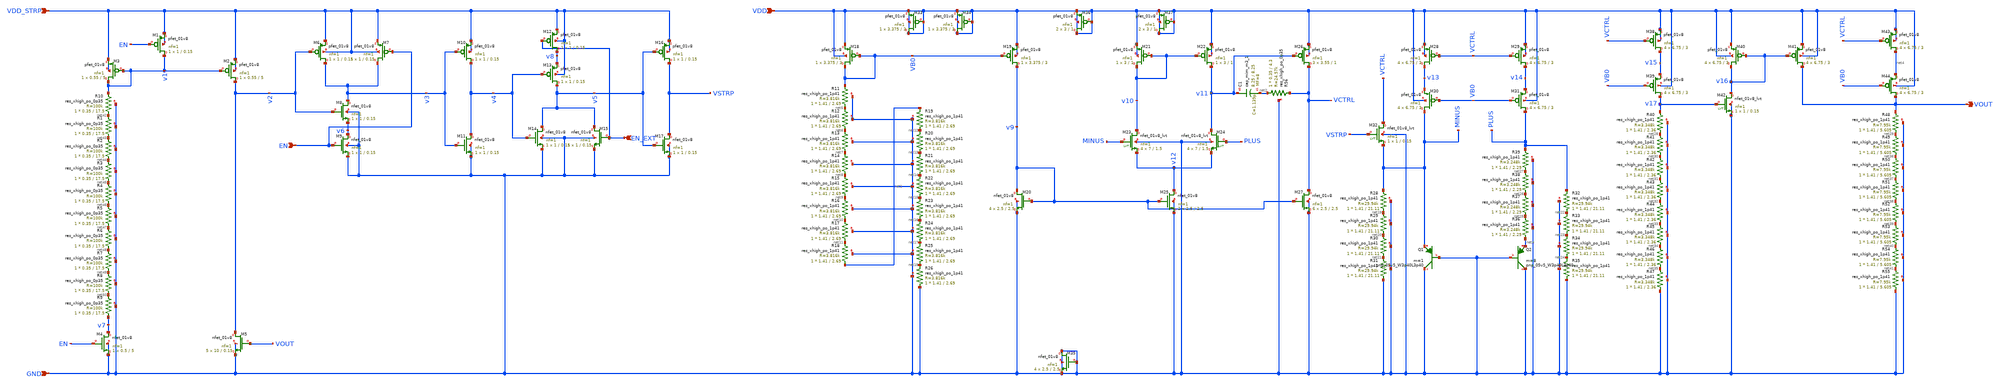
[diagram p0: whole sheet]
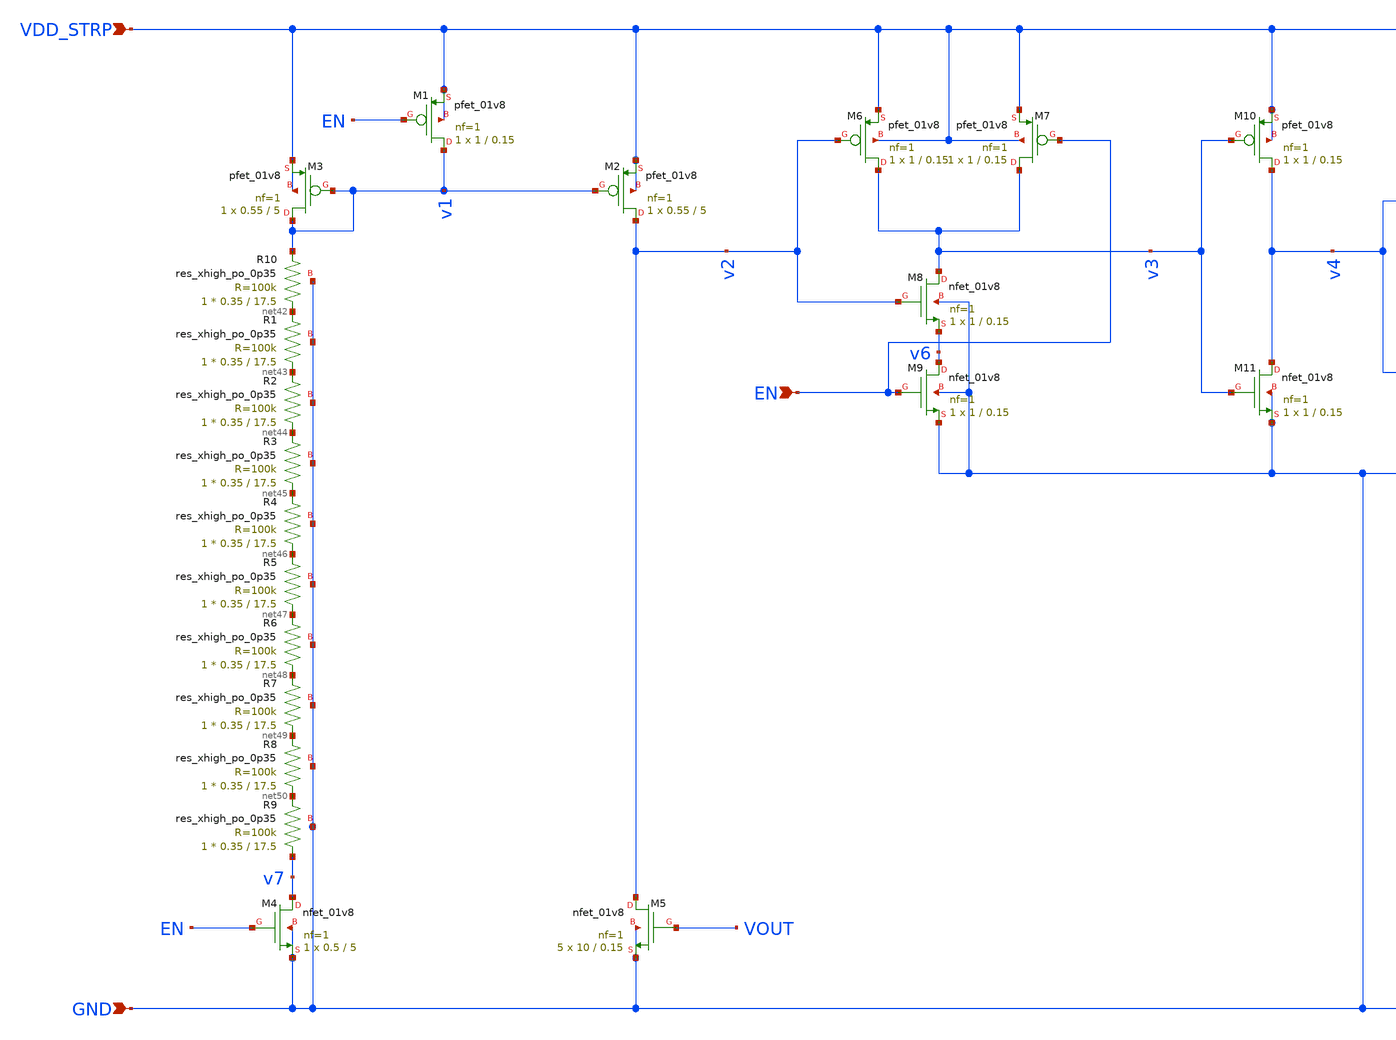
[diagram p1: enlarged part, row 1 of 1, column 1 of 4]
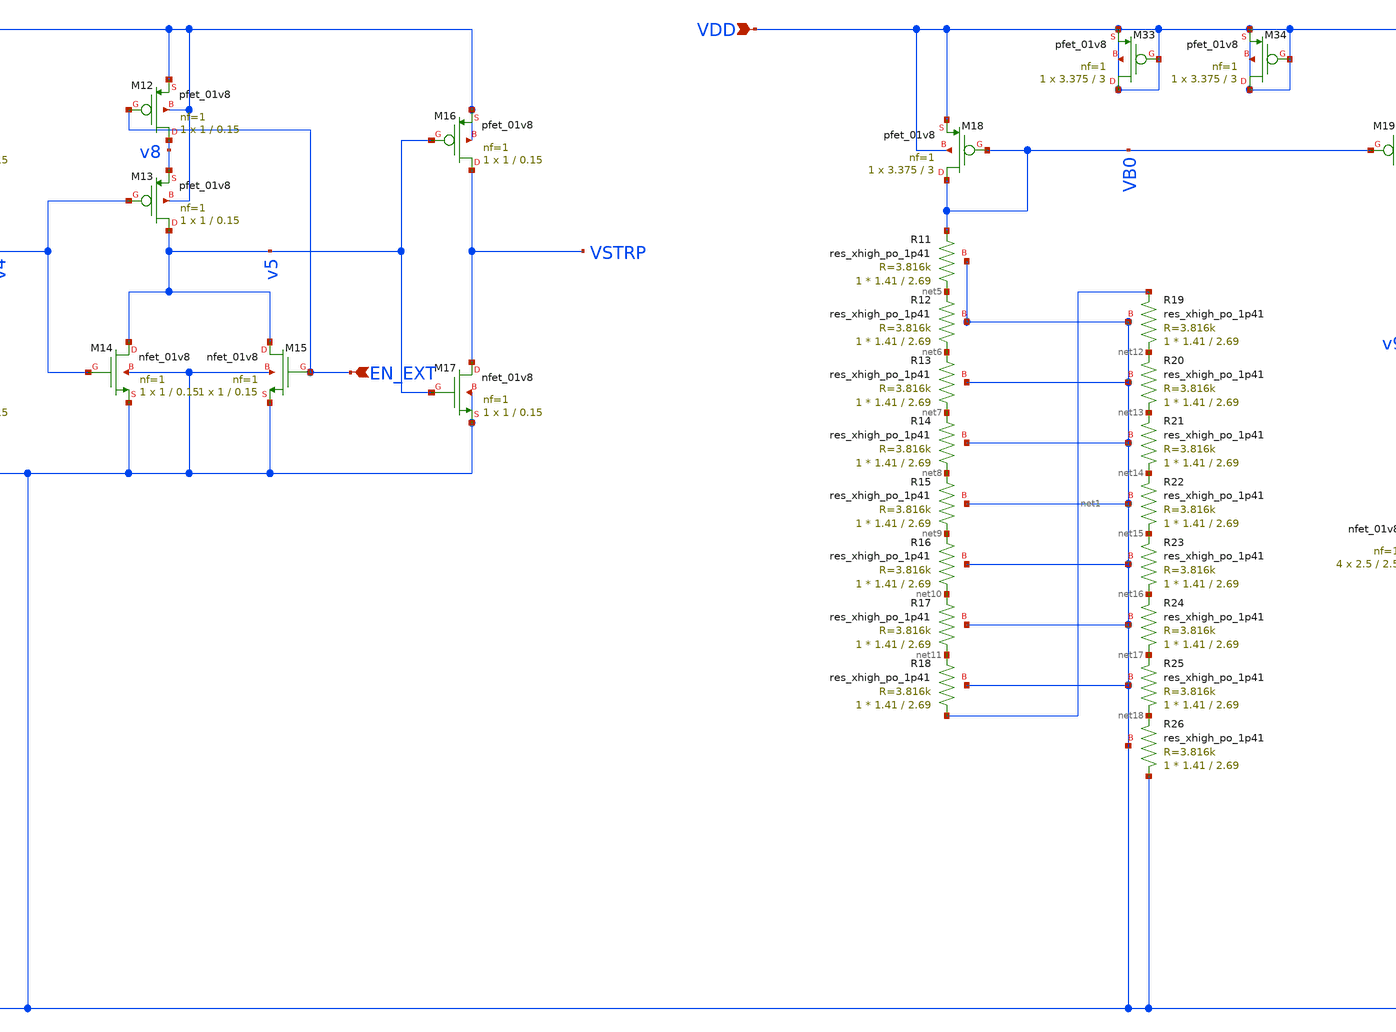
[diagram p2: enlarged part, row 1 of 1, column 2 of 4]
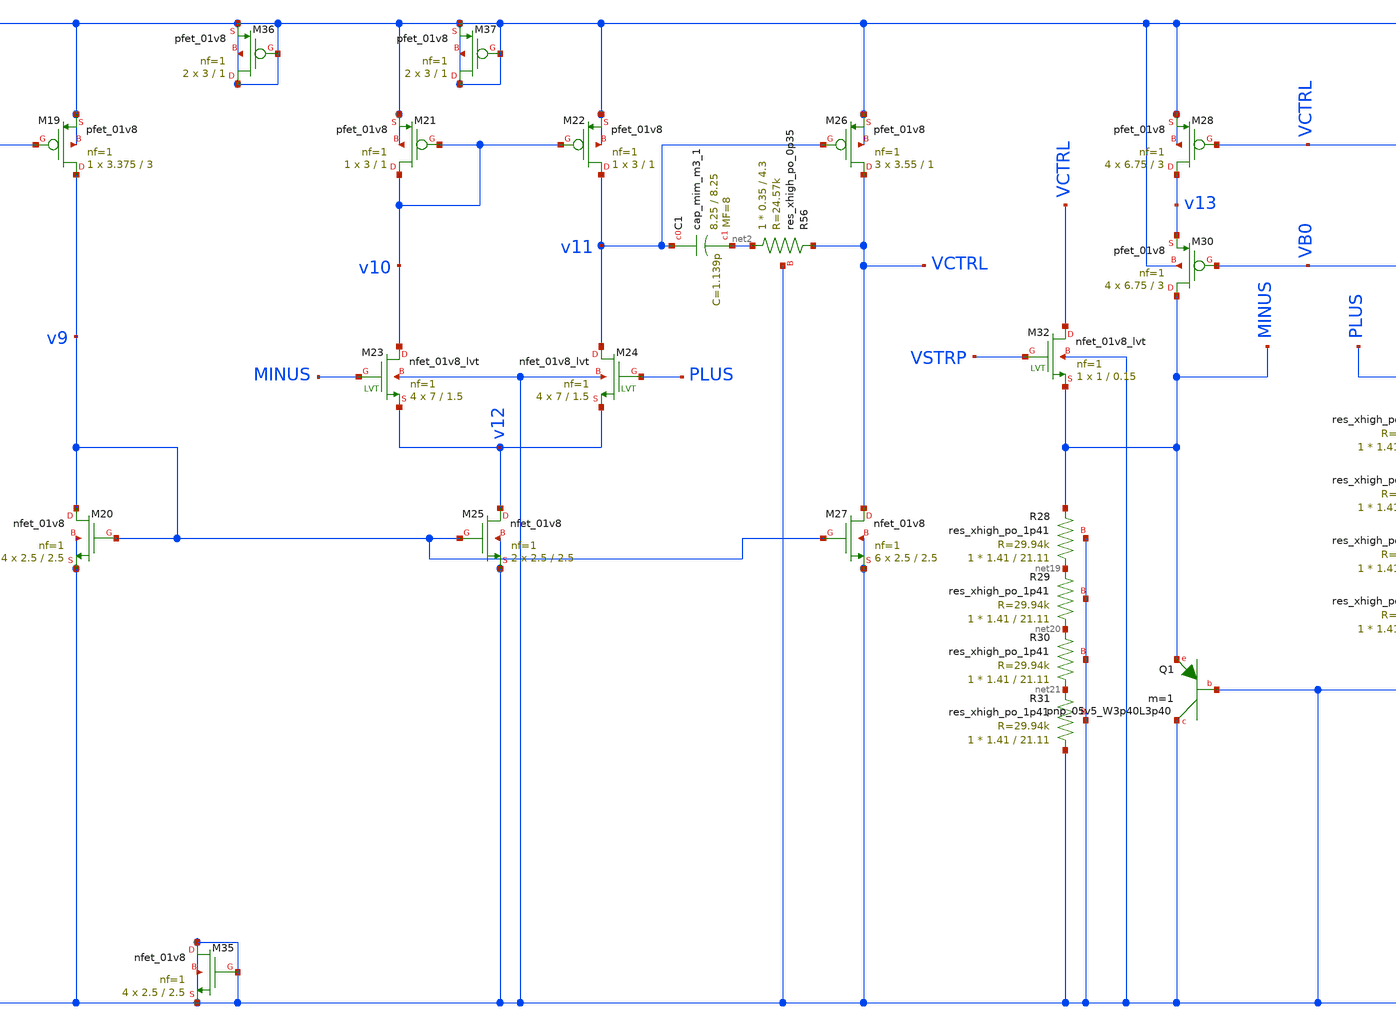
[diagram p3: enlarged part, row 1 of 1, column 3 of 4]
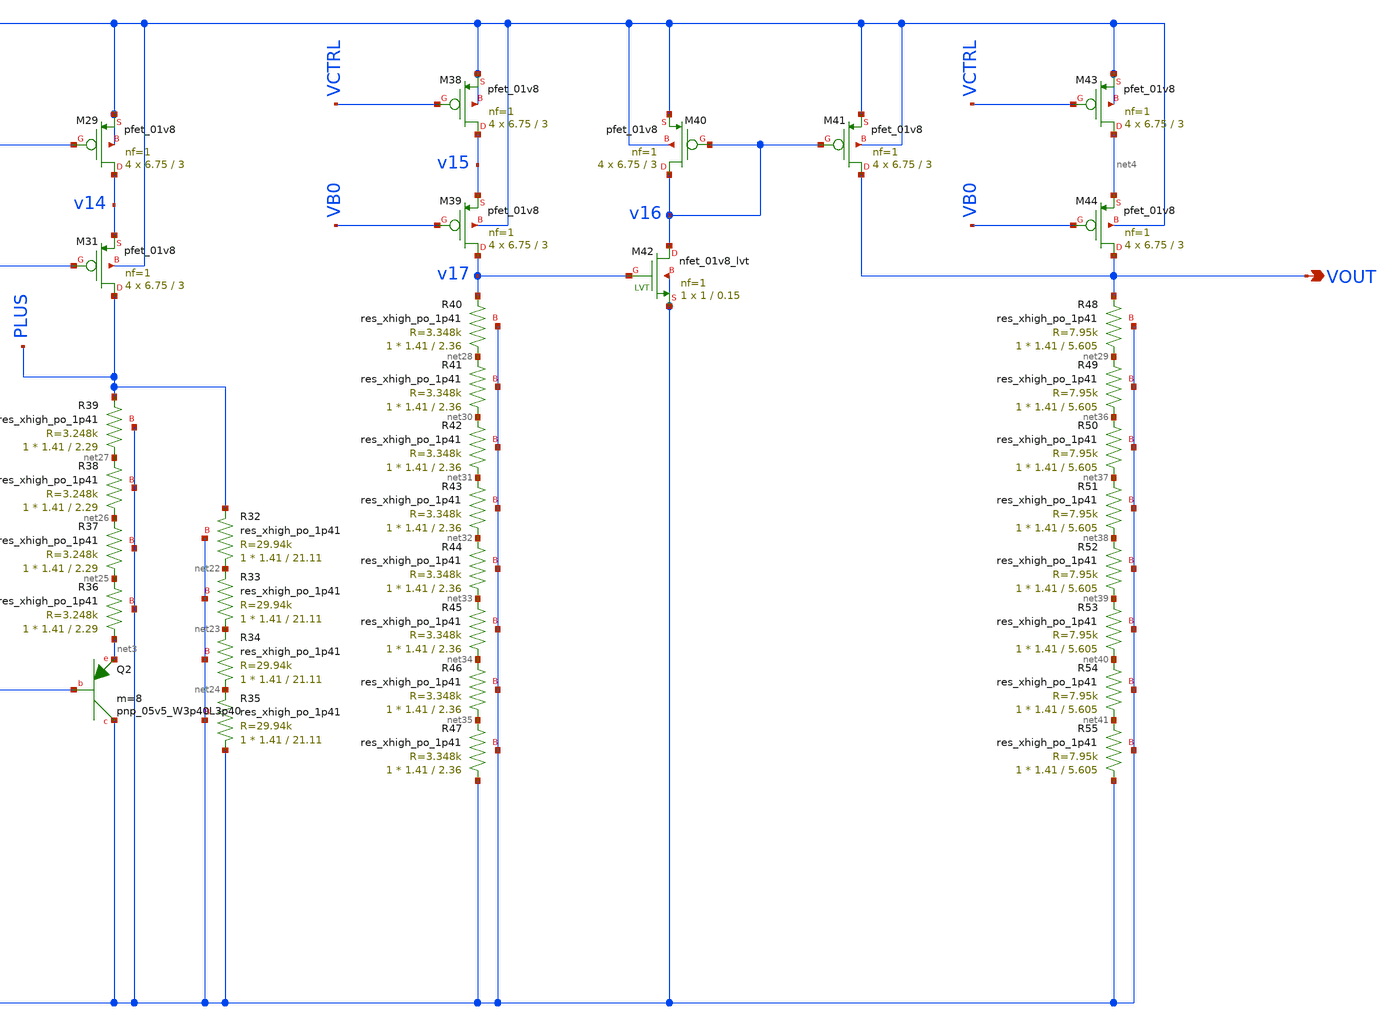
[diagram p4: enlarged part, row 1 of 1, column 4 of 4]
** sch_path: PBGR/PBGR.sch
**.subckt PBGR GND VDD_STRP VDD VOUT EN EN_EXT
*.ipin GND
*.ipin VDD_STRP
*.ipin VDD
*.opin VOUT
*.ipin EN
*.ipin EN_EXT
XM1 v1 EN VDD_STRP VDD_STRP sky130_fd_pr__pfet_01v8 L=0.15 W=1 nf=1 ad='int((nf+1)/2) * W/nf * 0.29'
+ as='int((nf+2)/2) * W/nf * 0.29' pd='2*int((nf+1)/2) * (W/nf + 0.29)' ps='2*int((nf+2)/2) * (W/nf + 0.29)'
+ nrd='0.29 / W' nrs='0.29 / W' sa=0 sb=0 sd=0 mult=1 m=1
XM2 v2 v1 VDD_STRP VDD_STRP sky130_fd_pr__pfet_01v8 L=5 W=0.55 nf=1 ad='int((nf+1)/2) * W/nf * 0.29'
+ as='int((nf+2)/2) * W/nf * 0.29' pd='2*int((nf+1)/2) * (W/nf + 0.29)' ps='2*int((nf+2)/2) * (W/nf + 0.29)'
+ nrd='0.29 / W' nrs='0.29 / W' sa=0 sb=0 sd=0 mult=1 m=1
XM3 v1 v1 VDD_STRP VDD_STRP sky130_fd_pr__pfet_01v8 L=5 W=0.55 nf=1 ad='int((nf+1)/2) * W/nf * 0.29'
+ as='int((nf+2)/2) * W/nf * 0.29' pd='2*int((nf+1)/2) * (W/nf + 0.29)' ps='2*int((nf+2)/2) * (W/nf + 0.29)'
+ nrd='0.29 / W' nrs='0.29 / W' sa=0 sb=0 sd=0 mult=1 m=1
XM4 v7 EN GND GND sky130_fd_pr__nfet_01v8 L=5 W=0.5 nf=1 ad='int((nf+1)/2) * W/nf * 0.29' as='int((nf+2)/2) * W/nf * 0.29'
+ pd='2*int((nf+1)/2) * (W/nf + 0.29)' ps='2*int((nf+2)/2) * (W/nf + 0.29)' nrd='0.29 / W' nrs='0.29 / W'
+ sa=0 sb=0 sd=0 mult=1 m=1
XM5 v2 VOUT GND GND sky130_fd_pr__nfet_01v8 L=0.15 W=10 nf=1 ad='int((nf+1)/2) * W/nf * 0.29' as='int((nf+2)/2) * W/nf * 0.29'
+ pd='2*int((nf+1)/2) * (W/nf + 0.29)' ps='2*int((nf+2)/2) * (W/nf + 0.29)' nrd='0.29 / W' nrs='0.29 / W'
+ sa=0 sb=0 sd=0 mult=5 m=5
XM6 v3 v2 VDD_STRP VDD_STRP sky130_fd_pr__pfet_01v8 L=0.15 W=1 nf=1 ad='int((nf+1)/2) * W/nf * 0.29'
+ as='int((nf+2)/2) * W/nf * 0.29' pd='2*int((nf+1)/2) * (W/nf + 0.29)' ps='2*int((nf+2)/2) * (W/nf + 0.29)'
+ nrd='0.29 / W' nrs='0.29 / W' sa=0 sb=0 sd=0 mult=1 m=1
XM7 v3 EN VDD_STRP VDD_STRP sky130_fd_pr__pfet_01v8 L=0.15 W=1 nf=1 ad='int((nf+1)/2) * W/nf * 0.29'
+ as='int((nf+2)/2) * W/nf * 0.29' pd='2*int((nf+1)/2) * (W/nf + 0.29)' ps='2*int((nf+2)/2) * (W/nf + 0.29)'
+ nrd='0.29 / W' nrs='0.29 / W' sa=0 sb=0 sd=0 mult=1 m=1
XM8 v3 v2 v6 GND sky130_fd_pr__nfet_01v8 L=0.15 W=1 nf=1 ad='int((nf+1)/2) * W/nf * 0.29' as='int((nf+2)/2) * W/nf * 0.29'
+ pd='2*int((nf+1)/2) * (W/nf + 0.29)' ps='2*int((nf+2)/2) * (W/nf + 0.29)' nrd='0.29 / W' nrs='0.29 / W'
+ sa=0 sb=0 sd=0 mult=1 m=1
XM9 v6 EN GND GND sky130_fd_pr__nfet_01v8 L=0.15 W=1 nf=1 ad='int((nf+1)/2) * W/nf * 0.29' as='int((nf+2)/2) * W/nf * 0.29'
+ pd='2*int((nf+1)/2) * (W/nf + 0.29)' ps='2*int((nf+2)/2) * (W/nf + 0.29)' nrd='0.29 / W' nrs='0.29 / W'
+ sa=0 sb=0 sd=0 mult=1 m=1
XM10 v4 v3 VDD_STRP VDD_STRP sky130_fd_pr__pfet_01v8 L=0.15 W=1 nf=1 ad='int((nf+1)/2) * W/nf * 0.29'
+ as='int((nf+2)/2) * W/nf * 0.29' pd='2*int((nf+1)/2) * (W/nf + 0.29)' ps='2*int((nf+2)/2) * (W/nf + 0.29)'
+ nrd='0.29 / W' nrs='0.29 / W' sa=0 sb=0 sd=0 mult=1 m=1
XM11 v4 v3 GND GND sky130_fd_pr__nfet_01v8 L=0.15 W=1 nf=1 ad='int((nf+1)/2) * W/nf * 0.29' as='int((nf+2)/2) * W/nf * 0.29'
+ pd='2*int((nf+1)/2) * (W/nf + 0.29)' ps='2*int((nf+2)/2) * (W/nf + 0.29)' nrd='0.29 / W' nrs='0.29 / W'
+ sa=0 sb=0 sd=0 mult=1 m=1
XM12 v8 EN_EXT VDD_STRP VDD_STRP sky130_fd_pr__pfet_01v8 L=0.15 W=1 nf=1 ad='int((nf+1)/2) * W/nf * 0.29'
+ as='int((nf+2)/2) * W/nf * 0.29' pd='2*int((nf+1)/2) * (W/nf + 0.29)' ps='2*int((nf+2)/2) * (W/nf + 0.29)'
+ nrd='0.29 / W' nrs='0.29 / W' sa=0 sb=0 sd=0 mult=1 m=1
XM13 v5 v4 v8 VDD_STRP sky130_fd_pr__pfet_01v8 L=0.15 W=1 nf=1 ad='int((nf+1)/2) * W/nf * 0.29' as='int((nf+2)/2) * W/nf * 0.29'
+ pd='2*int((nf+1)/2) * (W/nf + 0.29)' ps='2*int((nf+2)/2) * (W/nf + 0.29)' nrd='0.29 / W' nrs='0.29 / W'
+ sa=0 sb=0 sd=0 mult=1 m=1
XM14 v5 v4 GND GND sky130_fd_pr__nfet_01v8 L=0.15 W=1 nf=1 ad='int((nf+1)/2) * W/nf * 0.29' as='int((nf+2)/2) * W/nf * 0.29'
+ pd='2*int((nf+1)/2) * (W/nf + 0.29)' ps='2*int((nf+2)/2) * (W/nf + 0.29)' nrd='0.29 / W' nrs='0.29 / W'
+ sa=0 sb=0 sd=0 mult=1 m=1
XM15 v5 EN_EXT GND GND sky130_fd_pr__nfet_01v8 L=0.15 W=1 nf=1 ad='int((nf+1)/2) * W/nf * 0.29' as='int((nf+2)/2) * W/nf * 0.29'
+ pd='2*int((nf+1)/2) * (W/nf + 0.29)' ps='2*int((nf+2)/2) * (W/nf + 0.29)' nrd='0.29 / W' nrs='0.29 / W'
+ sa=0 sb=0 sd=0 mult=1 m=1
XM16 VSTRP v5 VDD_STRP VDD_STRP sky130_fd_pr__pfet_01v8 L=0.15 W=1 nf=1 ad='int((nf+1)/2) * W/nf * 0.29'
+ as='int((nf+2)/2) * W/nf * 0.29' pd='2*int((nf+1)/2) * (W/nf + 0.29)' ps='2*int((nf+2)/2) * (W/nf + 0.29)'
+ nrd='0.29 / W' nrs='0.29 / W' sa=0 sb=0 sd=0 mult=1 m=1
XM17 VSTRP v5 GND GND sky130_fd_pr__nfet_01v8 L=0.15 W=1 nf=1 ad='int((nf+1)/2) * W/nf * 0.29' as='int((nf+2)/2) * W/nf * 0.29'
+ pd='2*int((nf+1)/2) * (W/nf + 0.29)' ps='2*int((nf+2)/2) * (W/nf + 0.29)' nrd='0.29 / W' nrs='0.29 / W'
+ sa=0 sb=0 sd=0 mult=1 m=1
XM18 VB0 VB0 VDD VDD sky130_fd_pr__pfet_01v8 L=3 W=3.375 nf=1 ad='int((nf+1)/2) * W/nf * 0.29' as='int((nf+2)/2) * W/nf * 0.29'
+ pd='2*int((nf+1)/2) * (W/nf + 0.29)' ps='2*int((nf+2)/2) * (W/nf + 0.29)' nrd='0.29 / W' nrs='0.29 / W'
+ sa=0 sb=0 sd=0 mult=1 m=1
XR11 net5 VB0 GND sky130_fd_pr__res_xhigh_po_1p41 L=2.69 mult=1 m=1
XR12 net6 net5 GND sky130_fd_pr__res_xhigh_po_1p41 L=2.69 mult=1 m=1
XR13 net7 net6 GND sky130_fd_pr__res_xhigh_po_1p41 L=2.69 mult=1 m=1
XR14 net8 net7 GND sky130_fd_pr__res_xhigh_po_1p41 L=2.69 mult=1 m=1
XR15 net9 net8 GND sky130_fd_pr__res_xhigh_po_1p41 L=2.69 mult=1 m=1
XR16 net10 net9 GND sky130_fd_pr__res_xhigh_po_1p41 L=2.69 mult=1 m=1
XR17 net11 net10 GND sky130_fd_pr__res_xhigh_po_1p41 L=2.69 mult=1 m=1
XR18 net1 net11 GND sky130_fd_pr__res_xhigh_po_1p41 L=2.69 mult=1 m=1
XR19 net12 net1 GND sky130_fd_pr__res_xhigh_po_1p41 L=2.69 mult=1 m=1
XR20 net13 net12 GND sky130_fd_pr__res_xhigh_po_1p41 L=2.69 mult=1 m=1
XR21 net14 net13 GND sky130_fd_pr__res_xhigh_po_1p41 L=2.69 mult=1 m=1
XR22 net15 net14 GND sky130_fd_pr__res_xhigh_po_1p41 L=2.69 mult=1 m=1
XR23 net16 net15 GND sky130_fd_pr__res_xhigh_po_1p41 L=2.69 mult=1 m=1
XR24 net17 net16 GND sky130_fd_pr__res_xhigh_po_1p41 L=2.69 mult=1 m=1
XR25 net18 net17 GND sky130_fd_pr__res_xhigh_po_1p41 L=2.69 mult=1 m=1
XR26 GND net18 GND sky130_fd_pr__res_xhigh_po_1p41 L=2.69 mult=1 m=1
XM19 v9 VB0 VDD VDD sky130_fd_pr__pfet_01v8 L=3 W=3.375 nf=1 ad='int((nf+1)/2) * W/nf * 0.29' as='int((nf+2)/2) * W/nf * 0.29'
+ pd='2*int((nf+1)/2) * (W/nf + 0.29)' ps='2*int((nf+2)/2) * (W/nf + 0.29)' nrd='0.29 / W' nrs='0.29 / W'
+ sa=0 sb=0 sd=0 mult=1 m=1
XM20 v9 v9 GND GND sky130_fd_pr__nfet_01v8 L=2.5 W=2.5 nf=1 ad='int((nf+1)/2) * W/nf * 0.29' as='int((nf+2)/2) * W/nf * 0.29'
+ pd='2*int((nf+1)/2) * (W/nf + 0.29)' ps='2*int((nf+2)/2) * (W/nf + 0.29)' nrd='0.29 / W' nrs='0.29 / W'
+ sa=0 sb=0 sd=0 mult=4 m=4
XM21 v10 v10 VDD VDD sky130_fd_pr__pfet_01v8 L=1 W=3 nf=1 ad='int((nf+1)/2) * W/nf * 0.29' as='int((nf+2)/2) * W/nf * 0.29'
+ pd='2*int((nf+1)/2) * (W/nf + 0.29)' ps='2*int((nf+2)/2) * (W/nf + 0.29)' nrd='0.29 / W' nrs='0.29 / W'
+ sa=0 sb=0 sd=0 mult=1 m=1
XM22 v11 v10 VDD VDD sky130_fd_pr__pfet_01v8 L=1 W=3 nf=1 ad='int((nf+1)/2) * W/nf * 0.29' as='int((nf+2)/2) * W/nf * 0.29'
+ pd='2*int((nf+1)/2) * (W/nf + 0.29)' ps='2*int((nf+2)/2) * (W/nf + 0.29)' nrd='0.29 / W' nrs='0.29 / W'
+ sa=0 sb=0 sd=0 mult=1 m=1
XM24 v11 PLUS v12 GND sky130_fd_pr__nfet_01v8_lvt L=1.5 W=7 nf=1 ad='int((nf+1)/2) * W/nf * 0.29' as='int((nf+2)/2) * W/nf * 0.29'
+ pd='2*int((nf+1)/2) * (W/nf + 0.29)' ps='2*int((nf+2)/2) * (W/nf + 0.29)' nrd='0.29 / W' nrs='0.29 / W'
+ sa=0 sb=0 sd=0 mult=4 m=4
XM25 v12 v9 GND GND sky130_fd_pr__nfet_01v8 L=2.5 W=2.5 nf=1 ad='int((nf+1)/2) * W/nf * 0.29' as='int((nf+2)/2) * W/nf * 0.29'
+ pd='2*int((nf+1)/2) * (W/nf + 0.29)' ps='2*int((nf+2)/2) * (W/nf + 0.29)' nrd='0.29 / W' nrs='0.29 / W'
+ sa=0 sb=0 sd=0 mult=2 m=2
XM23 v10 MINUS v12 GND sky130_fd_pr__nfet_01v8_lvt L=1.5 W=7 nf=1 ad='int((nf+1)/2) * W/nf * 0.29' as='int((nf+2)/2) * W/nf * 0.29'
+ pd='2*int((nf+1)/2) * (W/nf + 0.29)' ps='2*int((nf+2)/2) * (W/nf + 0.29)' nrd='0.29 / W' nrs='0.29 / W'
+ sa=0 sb=0 sd=0 mult=4 m=4
XM26 VCTRL v11 VDD VDD sky130_fd_pr__pfet_01v8 L=1 W=3.55 nf=1 ad='int((nf+1)/2) * W/nf * 0.29' as='int((nf+2)/2) * W/nf * 0.29'
+ pd='2*int((nf+1)/2) * (W/nf + 0.29)' ps='2*int((nf+2)/2) * (W/nf + 0.29)' nrd='0.29 / W' nrs='0.29 / W'
+ sa=0 sb=0 sd=0 mult=3 m=3
XM27 VCTRL v9 GND GND sky130_fd_pr__nfet_01v8 L=2.5 W=2.5 nf=1 ad='int((nf+1)/2) * W/nf * 0.29' as='int((nf+2)/2) * W/nf * 0.29'
+ pd='2*int((nf+1)/2) * (W/nf + 0.29)' ps='2*int((nf+2)/2) * (W/nf + 0.29)' nrd='0.29 / W' nrs='0.29 / W'
+ sa=0 sb=0 sd=0 mult=6 m=6
XC1 v11 net2 sky130_fd_pr__cap_mim_m3_1 W=8.25 L=8.25 MF=8 m=8
XM28 v13 VCTRL VDD VDD sky130_fd_pr__pfet_01v8 L=3 W=6.75 nf=1 ad='int((nf+1)/2) * W/nf * 0.29' as='int((nf+2)/2) * W/nf * 0.29'
+ pd='2*int((nf+1)/2) * (W/nf + 0.29)' ps='2*int((nf+2)/2) * (W/nf + 0.29)' nrd='0.29 / W' nrs='0.29 / W'
+ sa=0 sb=0 sd=0 mult=4 m=4
XM29 v14 VCTRL VDD VDD sky130_fd_pr__pfet_01v8 L=3 W=6.75 nf=1 ad='int((nf+1)/2) * W/nf * 0.29' as='int((nf+2)/2) * W/nf * 0.29'
+ pd='2*int((nf+1)/2) * (W/nf + 0.29)' ps='2*int((nf+2)/2) * (W/nf + 0.29)' nrd='0.29 / W' nrs='0.29 / W'
+ sa=0 sb=0 sd=0 mult=4 m=4
XM30 MINUS VB0 v13 VDD sky130_fd_pr__pfet_01v8 L=3 W=6.75 nf=1 ad='int((nf+1)/2) * W/nf * 0.29' as='int((nf+2)/2) * W/nf * 0.29'
+ pd='2*int((nf+1)/2) * (W/nf + 0.29)' ps='2*int((nf+2)/2) * (W/nf + 0.29)' nrd='0.29 / W' nrs='0.29 / W'
+ sa=0 sb=0 sd=0 mult=4 m=4
XM31 PLUS VB0 v14 VDD sky130_fd_pr__pfet_01v8 L=3 W=6.75 nf=1 ad='int((nf+1)/2) * W/nf * 0.29' as='int((nf+2)/2) * W/nf * 0.29'
+ pd='2*int((nf+1)/2) * (W/nf + 0.29)' ps='2*int((nf+2)/2) * (W/nf + 0.29)' nrd='0.29 / W' nrs='0.29 / W'
+ sa=0 sb=0 sd=0 mult=4 m=4
XM32 VCTRL VSTRP MINUS GND sky130_fd_pr__nfet_01v8_lvt L=0.15 W=1 nf=1 ad='int((nf+1)/2) * W/nf * 0.29'
+ as='int((nf+2)/2) * W/nf * 0.29' pd='2*int((nf+1)/2) * (W/nf + 0.29)' ps='2*int((nf+2)/2) * (W/nf + 0.29)'
+ nrd='0.29 / W' nrs='0.29 / W' sa=0 sb=0 sd=0 mult=1 m=1
XM33 VDD VDD VDD VDD sky130_fd_pr__pfet_01v8 L=3 W=3.375 nf=1 ad='int((nf+1)/2) * W/nf * 0.29' as='int((nf+2)/2) * W/nf * 0.29'
+ pd='2*int((nf+1)/2) * (W/nf + 0.29)' ps='2*int((nf+2)/2) * (W/nf + 0.29)' nrd='0.29 / W' nrs='0.29 / W'
+ sa=0 sb=0 sd=0 mult=1 m=1
XM34 VDD VDD VDD VDD sky130_fd_pr__pfet_01v8 L=3 W=3.375 nf=1 ad='int((nf+1)/2) * W/nf * 0.29' as='int((nf+2)/2) * W/nf * 0.29'
+ pd='2*int((nf+1)/2) * (W/nf + 0.29)' ps='2*int((nf+2)/2) * (W/nf + 0.29)' nrd='0.29 / W' nrs='0.29 / W'
+ sa=0 sb=0 sd=0 mult=1 m=1
XM35 GND GND GND GND sky130_fd_pr__nfet_01v8 L=2.5 W=2.5 nf=1 ad='int((nf+1)/2) * W/nf * 0.29' as='int((nf+2)/2) * W/nf * 0.29'
+ pd='2*int((nf+1)/2) * (W/nf + 0.29)' ps='2*int((nf+2)/2) * (W/nf + 0.29)' nrd='0.29 / W' nrs='0.29 / W'
+ sa=0 sb=0 sd=0 mult=4 m=4
XM36 VDD VDD VDD VDD sky130_fd_pr__pfet_01v8 L=1 W=3 nf=1 ad='int((nf+1)/2) * W/nf * 0.29' as='int((nf+2)/2) * W/nf * 0.29'
+ pd='2*int((nf+1)/2) * (W/nf + 0.29)' ps='2*int((nf+2)/2) * (W/nf + 0.29)' nrd='0.29 / W' nrs='0.29 / W'
+ sa=0 sb=0 sd=0 mult=2 m=2
XM37 VDD VDD VDD VDD sky130_fd_pr__pfet_01v8 L=1 W=3 nf=1 ad='int((nf+1)/2) * W/nf * 0.29' as='int((nf+2)/2) * W/nf * 0.29'
+ pd='2*int((nf+1)/2) * (W/nf + 0.29)' ps='2*int((nf+2)/2) * (W/nf + 0.29)' nrd='0.29 / W' nrs='0.29 / W'
+ sa=0 sb=0 sd=0 mult=2 m=2
XR28 net19 MINUS GND sky130_fd_pr__res_xhigh_po_1p41 L=21.11 mult=1 m=1
XR29 net20 net19 GND sky130_fd_pr__res_xhigh_po_1p41 L=21.11 mult=1 m=1
XR30 net21 net20 GND sky130_fd_pr__res_xhigh_po_1p41 L=21.11 mult=1 m=1
XR31 GND net21 GND sky130_fd_pr__res_xhigh_po_1p41 L=21.11 mult=1 m=1
XR32 net22 PLUS GND sky130_fd_pr__res_xhigh_po_1p41 L=21.11 mult=1 m=1
XR33 net23 net22 GND sky130_fd_pr__res_xhigh_po_1p41 L=21.11 mult=1 m=1
XR34 net24 net23 GND sky130_fd_pr__res_xhigh_po_1p41 L=21.11 mult=1 m=1
XR35 GND net24 GND sky130_fd_pr__res_xhigh_po_1p41 L=21.11 mult=1 m=1
XQ1 GND GND MINUS sky130_fd_pr__pnp_05v5_W3p40L3p40 m=1
XQ2 GND GND net3 sky130_fd_pr__pnp_05v5_W3p40L3p40 m=8
XR36 net3 net25 GND sky130_fd_pr__res_xhigh_po_1p41 L=2.29 mult=1 m=1
XR37 net25 net26 GND sky130_fd_pr__res_xhigh_po_1p41 L=2.29 mult=1 m=1
XR38 net26 net27 GND sky130_fd_pr__res_xhigh_po_1p41 L=2.29 mult=1 m=1
XR39 net27 PLUS GND sky130_fd_pr__res_xhigh_po_1p41 L=2.29 mult=1 m=1
XR40 net28 v17 GND sky130_fd_pr__res_xhigh_po_1p41 L=2.36 mult=1 m=1
XM40 v16 v16 VDD VDD sky130_fd_pr__pfet_01v8 L=3 W=6.75 nf=1 ad='int((nf+1)/2) * W/nf * 0.29' as='int((nf+2)/2) * W/nf * 0.29'
+ pd='2*int((nf+1)/2) * (W/nf + 0.29)' ps='2*int((nf+2)/2) * (W/nf + 0.29)' nrd='0.29 / W' nrs='0.29 / W'
+ sa=0 sb=0 sd=0 mult=4 m=4
XM41 VOUT v16 VDD VDD sky130_fd_pr__pfet_01v8 L=3 W=6.75 nf=1 ad='int((nf+1)/2) * W/nf * 0.29' as='int((nf+2)/2) * W/nf * 0.29'
+ pd='2*int((nf+1)/2) * (W/nf + 0.29)' ps='2*int((nf+2)/2) * (W/nf + 0.29)' nrd='0.29 / W' nrs='0.29 / W'
+ sa=0 sb=0 sd=0 mult=4 m=4
XM42 v16 v17 GND GND sky130_fd_pr__nfet_01v8_lvt L=0.15 W=1 nf=1 ad='int((nf+1)/2) * W/nf * 0.29' as='int((nf+2)/2) * W/nf * 0.29'
+ pd='2*int((nf+1)/2) * (W/nf + 0.29)' ps='2*int((nf+2)/2) * (W/nf + 0.29)' nrd='0.29 / W' nrs='0.29 / W'
+ sa=0 sb=0 sd=0 mult=1 m=1
XR48 net29 VOUT GND sky130_fd_pr__res_xhigh_po_1p41 L=5.605 mult=1 m=1
XR41 net30 net28 GND sky130_fd_pr__res_xhigh_po_1p41 L=2.36 mult=1 m=1
XR42 net31 net30 GND sky130_fd_pr__res_xhigh_po_1p41 L=2.36 mult=1 m=1
XR43 net32 net31 GND sky130_fd_pr__res_xhigh_po_1p41 L=2.36 mult=1 m=1
XR44 net33 net32 GND sky130_fd_pr__res_xhigh_po_1p41 L=2.36 mult=1 m=1
XR45 net34 net33 GND sky130_fd_pr__res_xhigh_po_1p41 L=2.36 mult=1 m=1
XR46 net35 net34 GND sky130_fd_pr__res_xhigh_po_1p41 L=2.36 mult=1 m=1
XR47 GND net35 GND sky130_fd_pr__res_xhigh_po_1p41 L=2.36 mult=1 m=1
XM38 v15 VCTRL VDD VDD sky130_fd_pr__pfet_01v8 L=3 W=6.75 nf=1 ad='int((nf+1)/2) * W/nf * 0.29' as='int((nf+2)/2) * W/nf * 0.29'
+ pd='2*int((nf+1)/2) * (W/nf + 0.29)' ps='2*int((nf+2)/2) * (W/nf + 0.29)' nrd='0.29 / W' nrs='0.29 / W'
+ sa=0 sb=0 sd=0 mult=4 m=4
XM39 v17 VB0 v15 VDD sky130_fd_pr__pfet_01v8 L=3 W=6.75 nf=1 ad='int((nf+1)/2) * W/nf * 0.29' as='int((nf+2)/2) * W/nf * 0.29'
+ pd='2*int((nf+1)/2) * (W/nf + 0.29)' ps='2*int((nf+2)/2) * (W/nf + 0.29)' nrd='0.29 / W' nrs='0.29 / W'
+ sa=0 sb=0 sd=0 mult=4 m=4
XM43 net4 VCTRL VDD VDD sky130_fd_pr__pfet_01v8 L=3 W=6.75 nf=1 ad='int((nf+1)/2) * W/nf * 0.29' as='int((nf+2)/2) * W/nf * 0.29'
+ pd='2*int((nf+1)/2) * (W/nf + 0.29)' ps='2*int((nf+2)/2) * (W/nf + 0.29)' nrd='0.29 / W' nrs='0.29 / W'
+ sa=0 sb=0 sd=0 mult=4 m=4
XM44 VOUT VB0 net4 VDD sky130_fd_pr__pfet_01v8 L=3 W=6.75 nf=1 ad='int((nf+1)/2) * W/nf * 0.29' as='int((nf+2)/2) * W/nf * 0.29'
+ pd='2*int((nf+1)/2) * (W/nf + 0.29)' ps='2*int((nf+2)/2) * (W/nf + 0.29)' nrd='0.29 / W' nrs='0.29 / W'
+ sa=0 sb=0 sd=0 mult=4 m=4
XR49 net36 net29 GND sky130_fd_pr__res_xhigh_po_1p41 L=5.605 mult=1 m=1
XR50 net37 net36 GND sky130_fd_pr__res_xhigh_po_1p41 L=5.605 mult=1 m=1
XR51 net38 net37 GND sky130_fd_pr__res_xhigh_po_1p41 L=5.605 mult=1 m=1
XR52 net39 net38 GND sky130_fd_pr__res_xhigh_po_1p41 L=5.605 mult=1 m=1
XR53 net40 net39 GND sky130_fd_pr__res_xhigh_po_1p41 L=5.605 mult=1 m=1
XR54 net41 net40 GND sky130_fd_pr__res_xhigh_po_1p41 L=5.605 mult=1 m=1
XR55 GND net41 GND sky130_fd_pr__res_xhigh_po_1p41 L=5.605 mult=1 m=1
XR10 net42 v1 GND sky130_fd_pr__res_xhigh_po_0p35 L=17.5 mult=1 m=1
XR1 net43 net42 GND sky130_fd_pr__res_xhigh_po_0p35 L=17.5 mult=1 m=1
XR2 net44 net43 GND sky130_fd_pr__res_xhigh_po_0p35 L=17.5 mult=1 m=1
XR3 net45 net44 GND sky130_fd_pr__res_xhigh_po_0p35 L=17.5 mult=1 m=1
XR4 net46 net45 GND sky130_fd_pr__res_xhigh_po_0p35 L=17.5 mult=1 m=1
XR5 net47 net46 GND sky130_fd_pr__res_xhigh_po_0p35 L=17.5 mult=1 m=1
XR6 net48 net47 GND sky130_fd_pr__res_xhigh_po_0p35 L=17.5 mult=1 m=1
XR7 net49 net48 GND sky130_fd_pr__res_xhigh_po_0p35 L=17.5 mult=1 m=1
XR8 net50 net49 GND sky130_fd_pr__res_xhigh_po_0p35 L=17.5 mult=1 m=1
XR9 v7 net50 GND sky130_fd_pr__res_xhigh_po_0p35 L=17.5 mult=1 m=1
XR56 net2 VCTRL GND sky130_fd_pr__res_xhigh_po_0p35 L=4.3 mult=1 m=1
**.ends
.end
